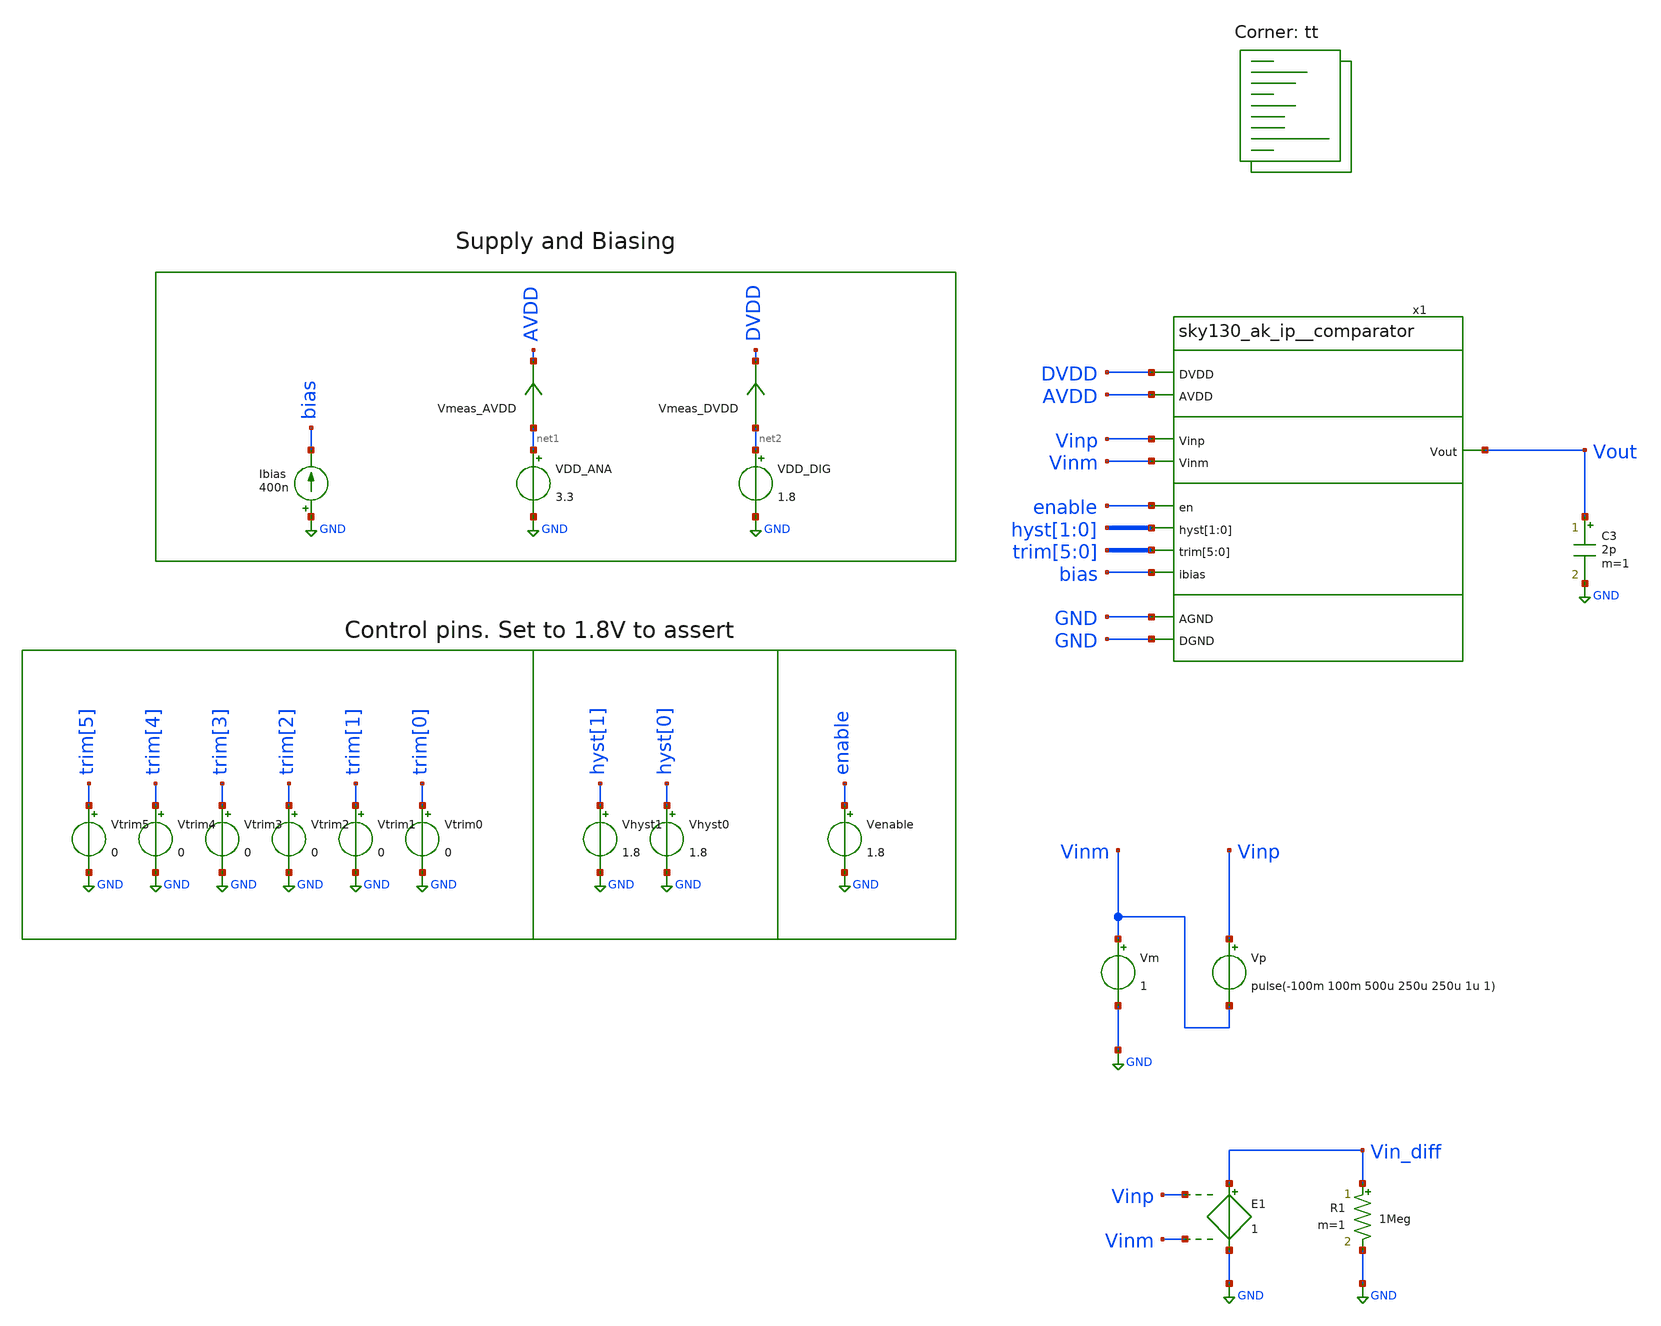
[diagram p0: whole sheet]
** sch_path: xschem/tb_comparator_hysteresis.sch
**.subckt tb_comparator_hysteresis
Vp Vinp Vinm pulse(-100m 100m 500u 250u 250u 1u 1)
VDD_ANA net1 GND 3.3
VDD_DIG net2 GND 1.8
Ibias GND bias 400n
C3 Vout GND 2p m=1
Vm Vinm GND 1
Vmeas_AVDD net1 AVDD 0
.save i(vmeas_avdd)
Vmeas_DVDD net2 DVDD 0
.save i(vmeas_dvdd)
E1 Vin_diff GND Vinp Vinm 1
Vtrim3 trim[3] GND 0
Vtrim2 trim[2] GND 0
Vtrim1 trim[1] GND 0
Vtrim0 trim[0] GND 0
Vhyst1 hyst[1] GND 1.8
Vhyst0 hyst[0] GND 1.8
Venable enable GND 1.8
Vtrim5 trim[5] GND 0
Vtrim4 trim[4] GND 0
x1 DVDD AVDD GND Vinp Vout Vinm enable hyst[1] hyst[0] trim[5] trim[4] trim[3] trim[2] trim[1]
+ trim[0] bias GND sky130_ak_ip__comparator
R1 Vin_diff GND 1Meg m=1
**** begin user architecture code
.lib $::SKYWATER_MODELS/sky130.lib.spice tt


.save v(vout) v(vin_diff)
.tran 100n 1m 500u uic
.ic v(x1.vop)=0 v(x1.vdiff)=1.8 v(x1.vout_int)=0 v(x1.voutb)=1.8 v(vout)=0 v(x1.trim0_hv)=0
+  v(x1.trim1_hv)=0 v(x1.trim2_hv)=0 v(x1.trim3_hv)=0 v(x1.trim4_hv)=0 v(x1.trim5_hv)=0  v(x1.enb_hv)=0
*.nodeset v(x1.vop)=0 v(x1.vdiff)=1.8 v(x1.vout_int)=0 v(x1.voutb)=1.8 v(x1.vout)=0

.control
let vec=unitvec(1)
let num_meas = 45
let input_offset_rise = unitvec(num_meas)
let input_offset_fall = unitvec(num_meas)
let i = 0
foreach temp_val -40 27 85
   set temp=$temp_val
   foreach vdd_ana_val 2.95 3.3 5.5
      alter VDD_ANA $vdd_ana_val
      foreach vm_val 1 {$vdd_ana_val/4} {$vdd_ana_val/2} {$vdd_ana_val*0.75} {-0.1+$vdd_ana_val}
         alter Vm $vm_val
         foreach ibias_val 400n
            alter ibias $ibias_val
            run
            meas tran t_cross_rise when v(vout)=0.9 rise=1
            meas tran in_cross_rise find v(vin_diff) at=t_cross_rise
            meas tran t_cross_fall when v(vout)=0.9 fall=1
            meas tran in_cross_fall find v(vin_diff) at=t_cross_fall
            let input_offset_rise[i] = in_cross_rise
            let input_offset_fall[i] = in_cross_fall
            let i = i+1
            set filetype = ascii
            set appendwrite
            set wr_singlescale
            setscale vec
            wrdata results_hysteresis_off.out in_cross_rise in_cross_fall
         end
      end
   end
end
*plot tran1.v(vout) tran2.v(vout) tran3.v(vout) tran4.v(vout) tran5.v(vout) tran6.v(vout)
*+ tran7.v(vout) tran8.v(vout) tran9.v(vout) tran10.v(vout) tran11.v(vout) tran12.v(vout) tran13.v(vout)
*+ tran14.v(vout) tran15.v(vout) tran16.v(vout) tran16.v(vout) tran17.v(vout) tran18.v(vout)
*plot dc1.v(vout) dc2.v(vout) dc3.v(vout) dc4.v(vout) dc5.v(vout) dc6.v(vout) dc7.v(vout)
*+ dc8.v(vout) dc9.v(vout) dc10.v(vout) dc11.v(vout) dc12.v(vout) dc13.v(vout) dc14.v(vout) dc15.v(vout)
*+ dc16.v(vout) dc17.v(vout) dc18.v(vout) dc19.v(vout) dc20.v(vout) dc21.v(vout) dc22.v(vout) dc23.v(vout)
*+ dc24.v(vout) dc25.v(vout) dc26.v(vout) dc27.v(vout)
*plot tran1.v(vin_diff)
set filetype = ascii
*write results_hysteresis_off_rising_fs.raw input_offset_rise
*write results_hysteresis_off_falling_fs.raw input_offset_fall
print vecmin(input_offset_rise)
print vecmax(input_offset_rise)
print vecmin(input_offset_fall)
print vecmax(input_offset_fall)
.endc


**** end user architecture code
**.ends
.GLOBAL GND
.end
